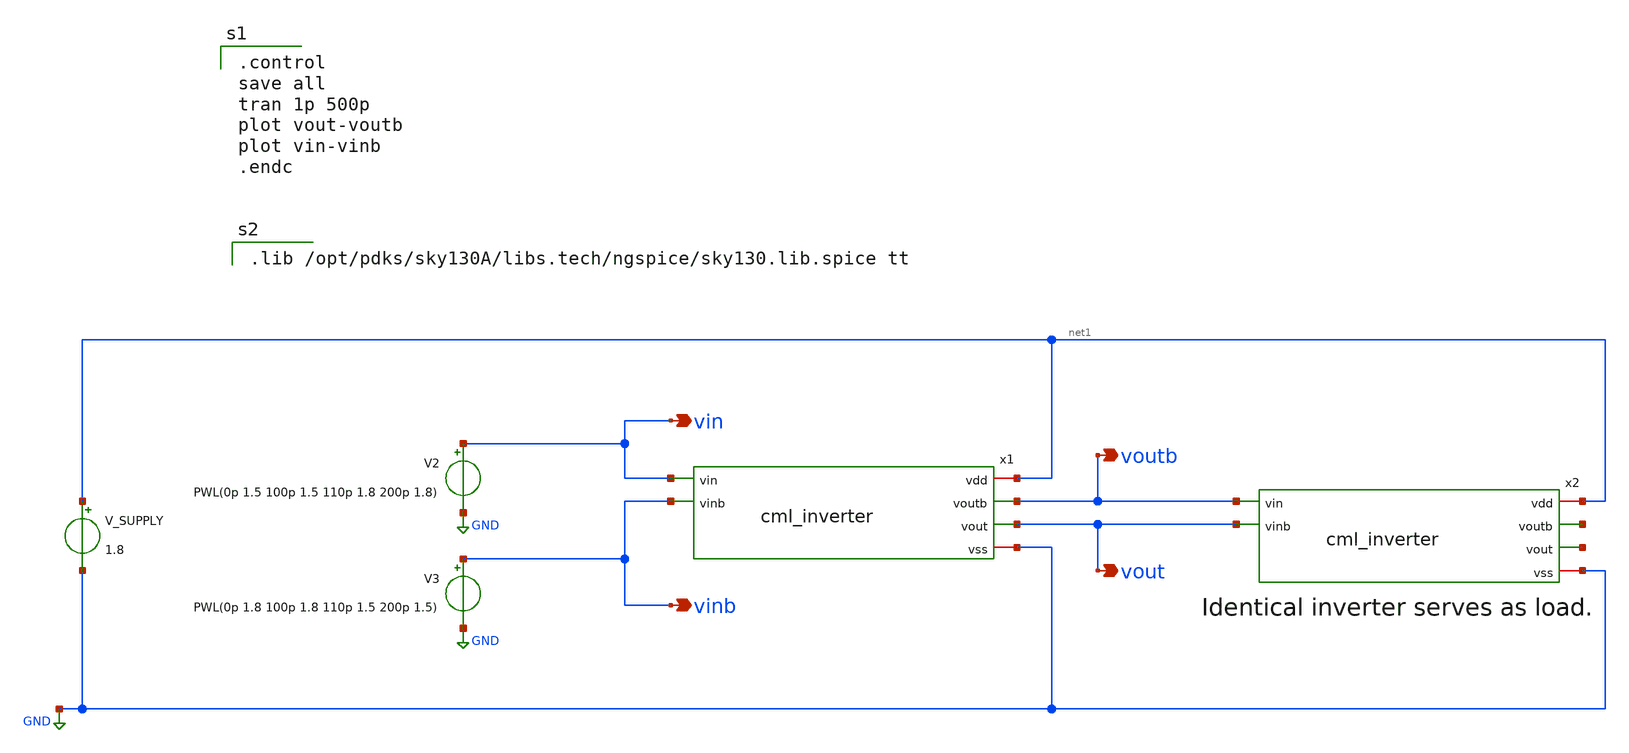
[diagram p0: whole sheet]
** sch_path: xschem/cml_inverter_tb.sch
**.subckt cml_inverter_tb voutb vout vin vinb
*.opin voutb
*.opin vout
*.opin vin
*.opin vinb
x1 net1 voutb vout vin vinb GND cml_inverter
V_SUPPLY net1 GND 1.8
V2 vin GND PWL(0p 1.5 100p 1.5 110p 1.8 200p 1.8)
V3 vinb GND PWL(0p 1.8 100p 1.8 110p 1.5 200p 1.5)
x2 net1 net2 net3 voutb vout GND cml_inverter
**** begin user architecture code

.control
save all
tran 1p 500p
plot vout-voutb
plot vin-vinb
.endc


.lib /opt/pdks/sky130A/libs.tech/ngspice/sky130.lib.spice tt

**** end user architecture code
**.ends

* expanding   symbol:  cml_inverter.sym # of pins=6
** sym_path: xschem/cml_inverter.sym
** sch_path: xschem/cml_inverter.sch
.subckt cml_inverter vdd voutb vout vin vinb vss
*.ipin vinb
*.ipin vin
*.iopin vdd
*.iopin vss
*.opin vout
*.opin voutb
ISS net1 vss 1m
R1 vdd vout 300 m=1
R2 vdd voutb 300 m=1
XM1 vout vinb net1 vss sky130_fd_pr__nfet_01v8 L=0.15 W=18 nf=1 ad='int((nf+1)/2) * W/nf * 0.29' as='int((nf+2)/2) * W/nf * 0.29'
+ pd='2*int((nf+1)/2) * (W/nf + 0.29)' ps='2*int((nf+2)/2) * (W/nf + 0.29)' nrd='0.29 / W' nrs='0.29 / W'
+ sa=0 sb=0 sd=0 mult=1 m=1
XM2 voutb vin net1 vss sky130_fd_pr__nfet_01v8 L=0.15 W=18 nf=1 ad='int((nf+1)/2) * W/nf * 0.29' as='int((nf+2)/2) * W/nf * 0.29'
+ pd='2*int((nf+1)/2) * (W/nf + 0.29)' ps='2*int((nf+2)/2) * (W/nf + 0.29)' nrd='0.29 / W' nrs='0.29 / W'
+ sa=0 sb=0 sd=0 mult=1 m=1
.ends

.GLOBAL GND
.end
